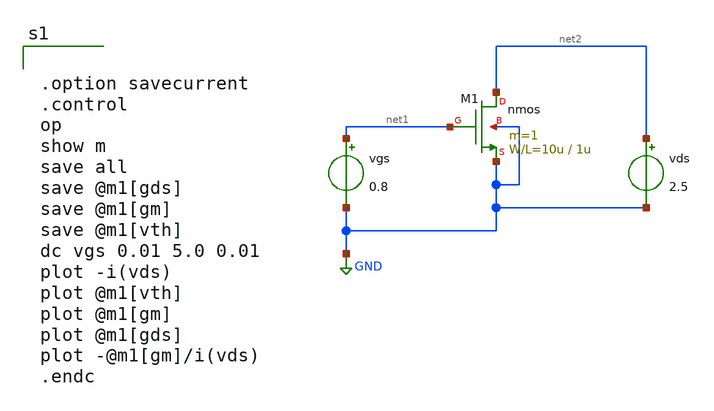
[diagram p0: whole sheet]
** sch_path: member_project/GroupWork/Team_masahiro/nfet_id-vgs.sch
**.subckt nfet_id-vgs
vgs net1 GND 0.8
vds net2 GND 2.5
M1 net2 net1 GND GND nmos L=1u W=10u m=1
**** begin user architecture code
 .include $::LIB/mos.lib
.include $::LIB/passive.lib
.include $::LIB/diode.lib


.option savecurrent
.control
op
show m
save all
save @m1[gds]
save @m1[gm]
save @m1[vth]
dc vgs 0.01 5.0 0.01
plot -i(vds)
plot @m1[vth]
plot @m1[gm]
plot @m1[gds]
plot -@m1[gm]/i(vds)
.endc


**** end user architecture code
**.ends
.GLOBAL GND
.end
